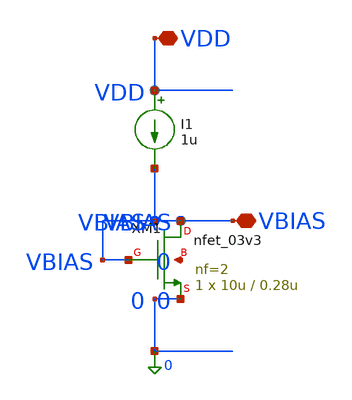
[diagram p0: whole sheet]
** sch_path: modules/PandaChip/designs/iris-harvester/exp/bias.sch
**.subckt bias VDD VBIAS
*.iopin VDD
*.iopin VBIAS
I1 VDD VBIAS 1u
XM1 VBIAS VBIAS 0 0 nfet_03v3 L=0.28u W=10u nf=2 ad='int((nf+1)/2) * W/nf * 0.18u' as='int((nf+2)/2) * W/nf * 0.18u'
+ pd='2*int((nf+1)/2) * (W/nf + 0.18u)' ps='2*int((nf+2)/2) * (W/nf + 0.18u)' nrd='0.18u / W' nrs='0.18u / W'
+ sa=0 sb=0 sd=0 m=1
**.ends
.end
